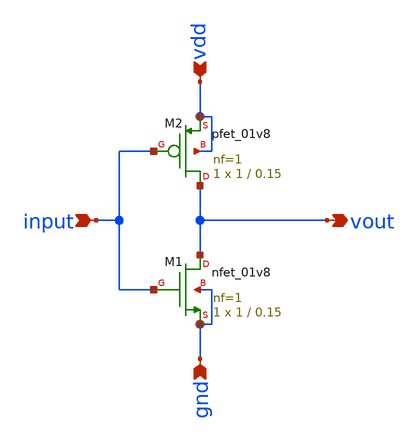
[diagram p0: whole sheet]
** sch_path: analog/schematics/test_invertor.sch
**.subckt test_invertor input gnd vdd vout
*.ipin input
*.ipin gnd
*.ipin vdd
*.opin vout
XM1 vout input gnd gnd sky130_fd_pr__nfet_01v8 L=0.15 W=1 nf=1 ad='int((nf+1)/2) * W/nf * 0.29' as='int((nf+2)/2) * W/nf * 0.29'
+ pd='2*int((nf+1)/2) * (W/nf + 0.29)' ps='2*int((nf+2)/2) * (W/nf + 0.29)' nrd='0.29 / W' nrs='0.29 / W'
+ sa=0 sb=0 sd=0 mult=1 m=1
XM2 vout input vdd vdd sky130_fd_pr__pfet_01v8 L=0.15 W=1 nf=1 ad='int((nf+1)/2) * W/nf * 0.29' as='int((nf+2)/2) * W/nf * 0.29'
+ pd='2*int((nf+1)/2) * (W/nf + 0.29)' ps='2*int((nf+2)/2) * (W/nf + 0.29)' nrd='0.29 / W' nrs='0.29 / W'
+ sa=0 sb=0 sd=0 mult=1 m=1
**.ends
.end
